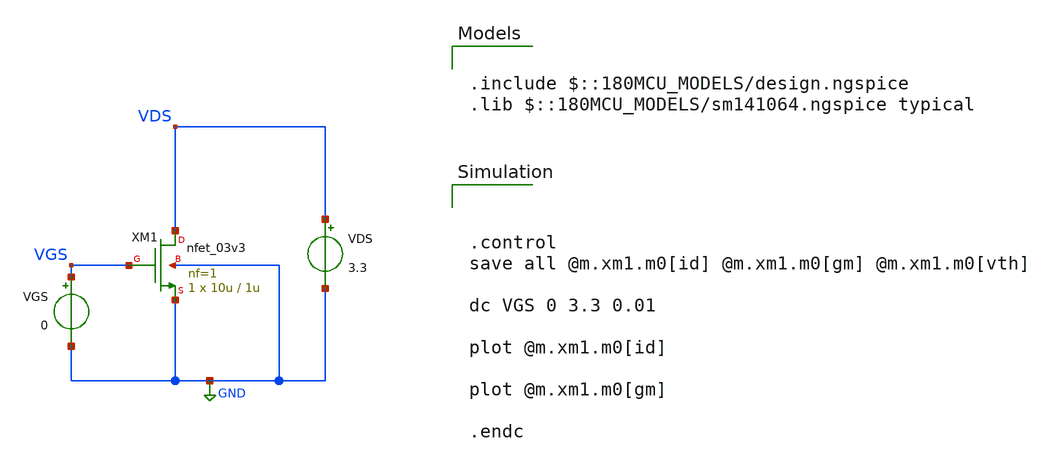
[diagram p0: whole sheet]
** sch_path: designs/libs/session_1/nmos_id_vgs.sch
**.subckt nmos_id_vgs
XM1 VDS VGS GND GND nfet_03v3 L=1u W=10u nf=1 ad='int((nf+1)/2) * W/nf * 0.18u' as='int((nf+2)/2) * W/nf * 0.18u'
+ pd='2*int((nf+1)/2) * (W/nf + 0.18u)' ps='2*int((nf+2)/2) * (W/nf + 0.18u)' nrd='0.18u / W' nrs='0.18u / W'
+ sa=0 sb=0 sd=0 m=1
VDS VDS GND 3.3
VGS VGS GND 0
**** begin user architecture code



.control
save all @m.xm1.m0[id] @m.xm1.m0[gm] @m.xm1.m0[vth]

dc VGS 0 3.3 0.01

plot @m.xm1.m0[id]

plot @m.xm1.m0[gm]

.endc




.include $::180MCU_MODELS/design.ngspice
.lib $::180MCU_MODELS/sm141064.ngspice typical

**** end user architecture code
**.ends
.GLOBAL GND
.end
